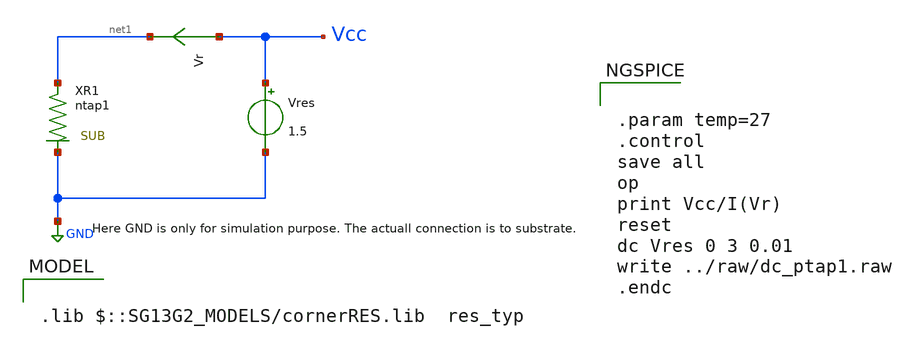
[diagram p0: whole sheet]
** sch_path: ihp-sg13g2/libs.tech/xschem/sg13g2_tests/dc_ptap1.sch
* Copyright 2023 IHP PDK Authors
**.subckt dc_ptap1
Vres Vcc GND 1.5
XR1 GND net1 ntap1
Vr Vcc net1 0
.save i(vr)
**** begin user architecture code

.lib $::SG13G2_MODELS/cornerRES.lib  res_typ



.param temp=27
.control
save all
op
print Vcc/I(Vr)
reset
dc Vres 0 3 0.01
write ../raw/dc_ptap1.raw
.endc


**** end user architecture code
**.ends
.GLOBAL GND
.end
